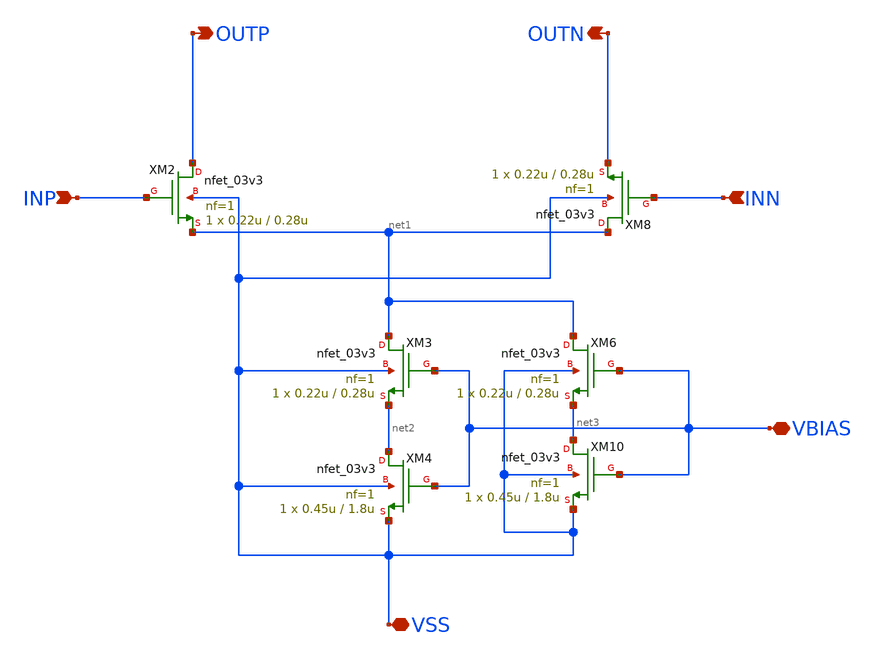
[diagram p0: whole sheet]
** sch_path: xschem/CS_Switch_4x2.sch
**.subckt CS_Switch_4x2 INP INN OUTP OUTN VBIAS VSS
*.ipin INP
*.ipin INN
*.opin OUTP
*.opin OUTN
*.iopin VBIAS
*.iopin VSS
XM2 OUTP INP net1 VSS nfet_03v3 L=0.28u W=0.22u nf=1 ad='int((nf+1)/2) * W/nf * 0.18u' as='int((nf+2)/2) * W/nf * 0.18u'
+ pd='2*int((nf+1)/2) * (W/nf + 0.18u)' ps='2*int((nf+2)/2) * (W/nf + 0.18u)' nrd='0.18u / W' nrs='0.18u / W'
+ sa=0 sb=0 sd=0 m=1
XM3 net1 VBIAS net2 VSS nfet_03v3 L=0.28u W=0.22u nf=1 ad='int((nf+1)/2) * W/nf * 0.18u' as='int((nf+2)/2) * W/nf * 0.18u'
+ pd='2*int((nf+1)/2) * (W/nf + 0.18u)' ps='2*int((nf+2)/2) * (W/nf + 0.18u)' nrd='0.18u / W' nrs='0.18u / W'
+ sa=0 sb=0 sd=0 m=1
XM4 net2 VBIAS VSS VSS nfet_03v3 L=1.8u W=0.45u nf=1 ad='int((nf+1)/2) * W/nf * 0.18u' as='int((nf+2)/2) * W/nf * 0.18u'
+ pd='2*int((nf+1)/2) * (W/nf + 0.18u)' ps='2*int((nf+2)/2) * (W/nf + 0.18u)' nrd='0.18u / W' nrs='0.18u / W'
+ sa=0 sb=0 sd=0 m=1
XM6 net1 VBIAS net3 VSS nfet_03v3 L=0.28u W=0.22u nf=1 ad='int((nf+1)/2) * W/nf * 0.18u' as='int((nf+2)/2) * W/nf * 0.18u'
+ pd='2*int((nf+1)/2) * (W/nf + 0.18u)' ps='2*int((nf+2)/2) * (W/nf + 0.18u)' nrd='0.18u / W' nrs='0.18u / W'
+ sa=0 sb=0 sd=0 m=1
XM8 net1 INN OUTN VSS nfet_03v3 L=0.28u W=0.22u nf=1 ad='int((nf+1)/2) * W/nf * 0.18u' as='int((nf+2)/2) * W/nf * 0.18u'
+ pd='2*int((nf+1)/2) * (W/nf + 0.18u)' ps='2*int((nf+2)/2) * (W/nf + 0.18u)' nrd='0.18u / W' nrs='0.18u / W'
+ sa=0 sb=0 sd=0 m=1
XM10 net3 VBIAS VSS VSS nfet_03v3 L=1.8u W=0.45u nf=1 ad='int((nf+1)/2) * W/nf * 0.18u' as='int((nf+2)/2) * W/nf * 0.18u'
+ pd='2*int((nf+1)/2) * (W/nf + 0.18u)' ps='2*int((nf+2)/2) * (W/nf + 0.18u)' nrd='0.18u / W' nrs='0.18u / W'
+ sa=0 sb=0 sd=0 m=1
**.ends
.end
